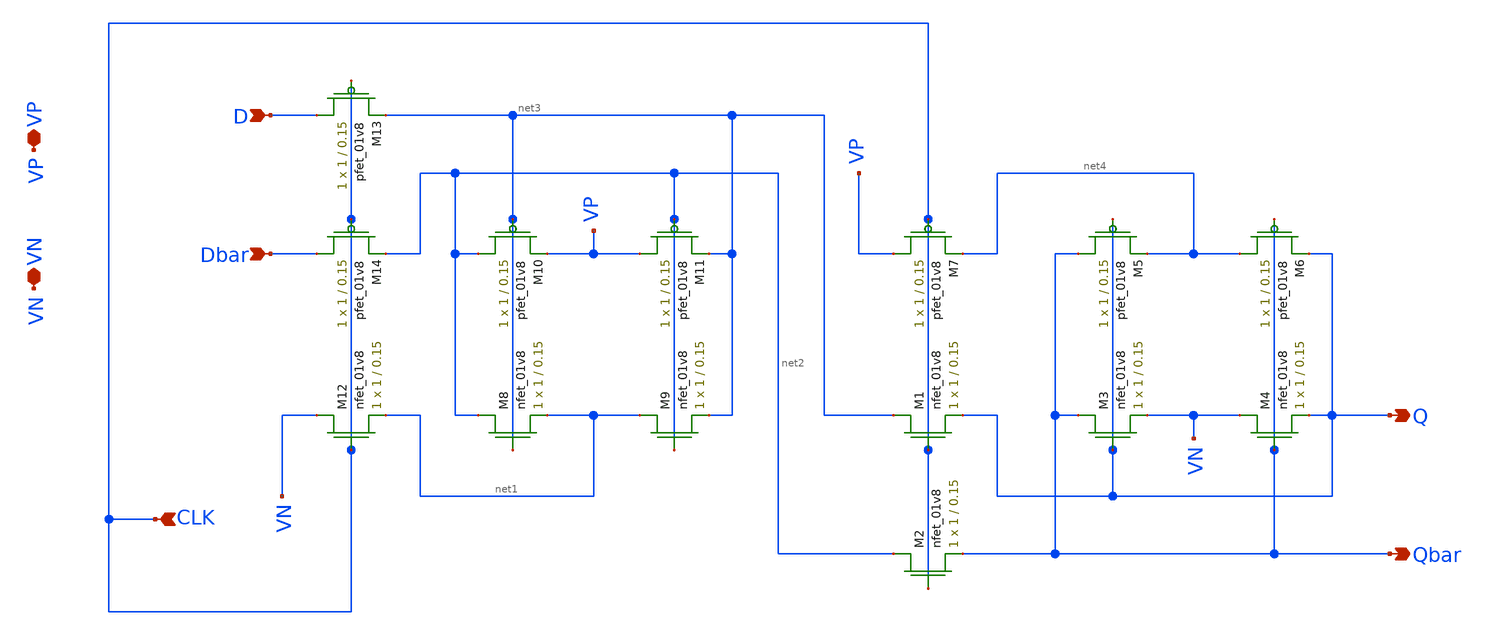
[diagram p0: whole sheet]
** sch_path: mp2/xschem/flipflop/flipflop_layout.sch
**.subckt flipflop_layout D Dbar Q Qbar CLK VP VN
*.ipin D
*.ipin Dbar
*.opin Q
*.opin Qbar
*.ipin CLK
*.iopin VP
*.iopin VN
XM1 net3 CLK Q GND sky130_fd_pr__nfet_01v8 L=0.15 W=1 nf=1 ad='int((nf+1)/2) * W/nf * 0.29' as='int((nf+2)/2) * W/nf * 0.29'
+ pd='2*int((nf+1)/2) * (W/nf + 0.29)' ps='2*int((nf+2)/2) * (W/nf + 0.29)' nrd='0.29 / W' nrs='0.29 / W'
+ sa=0 sb=0 sd=0 mult=1 m=1
XM2 net2 CLK Qbar GND sky130_fd_pr__nfet_01v8 L=0.15 W=1 nf=1 ad='int((nf+1)/2) * W/nf * 0.29' as='int((nf+2)/2) * W/nf * 0.29'
+ pd='2*int((nf+1)/2) * (W/nf + 0.29)' ps='2*int((nf+2)/2) * (W/nf + 0.29)' nrd='0.29 / W' nrs='0.29 / W'
+ sa=0 sb=0 sd=0 mult=1 m=1
XM3 Qbar Q VN GND sky130_fd_pr__nfet_01v8 L=0.15 W=1 nf=1 ad='int((nf+1)/2) * W/nf * 0.29' as='int((nf+2)/2) * W/nf * 0.29'
+ pd='2*int((nf+1)/2) * (W/nf + 0.29)' ps='2*int((nf+2)/2) * (W/nf + 0.29)' nrd='0.29 / W' nrs='0.29 / W'
+ sa=0 sb=0 sd=0 mult=1 m=1
XM4 VN Qbar Q GND sky130_fd_pr__nfet_01v8 L=0.15 W=1 nf=1 ad='int((nf+1)/2) * W/nf * 0.29' as='int((nf+2)/2) * W/nf * 0.29'
+ pd='2*int((nf+1)/2) * (W/nf + 0.29)' ps='2*int((nf+2)/2) * (W/nf + 0.29)' nrd='0.29 / W' nrs='0.29 / W'
+ sa=0 sb=0 sd=0 mult=1 m=1
XM5 Qbar Q net4 VDD sky130_fd_pr__pfet_01v8 L=0.15 W=1 nf=1 ad='int((nf+1)/2) * W/nf * 0.29' as='int((nf+2)/2) * W/nf * 0.29'
+ pd='2*int((nf+1)/2) * (W/nf + 0.29)' ps='2*int((nf+2)/2) * (W/nf + 0.29)' nrd='0.29 / W' nrs='0.29 / W'
+ sa=0 sb=0 sd=0 mult=1 m=1
XM6 net4 Qbar Q VDD sky130_fd_pr__pfet_01v8 L=0.15 W=1 nf=1 ad='int((nf+1)/2) * W/nf * 0.29' as='int((nf+2)/2) * W/nf * 0.29'
+ pd='2*int((nf+1)/2) * (W/nf + 0.29)' ps='2*int((nf+2)/2) * (W/nf + 0.29)' nrd='0.29 / W' nrs='0.29 / W'
+ sa=0 sb=0 sd=0 mult=1 m=1
XM7 VP CLK net4 VDD sky130_fd_pr__pfet_01v8 L=0.15 W=1 nf=1 ad='int((nf+1)/2) * W/nf * 0.29' as='int((nf+2)/2) * W/nf * 0.29'
+ pd='2*int((nf+1)/2) * (W/nf + 0.29)' ps='2*int((nf+2)/2) * (W/nf + 0.29)' nrd='0.29 / W' nrs='0.29 / W'
+ sa=0 sb=0 sd=0 mult=1 m=1
XM8 net2 net3 net1 GND sky130_fd_pr__nfet_01v8 L=0.15 W=1 nf=1 ad='int((nf+1)/2) * W/nf * 0.29' as='int((nf+2)/2) * W/nf * 0.29'
+ pd='2*int((nf+1)/2) * (W/nf + 0.29)' ps='2*int((nf+2)/2) * (W/nf + 0.29)' nrd='0.29 / W' nrs='0.29 / W'
+ sa=0 sb=0 sd=0 mult=1 m=1
XM9 net1 net2 net3 GND sky130_fd_pr__nfet_01v8 L=0.15 W=1 nf=1 ad='int((nf+1)/2) * W/nf * 0.29' as='int((nf+2)/2) * W/nf * 0.29'
+ pd='2*int((nf+1)/2) * (W/nf + 0.29)' ps='2*int((nf+2)/2) * (W/nf + 0.29)' nrd='0.29 / W' nrs='0.29 / W'
+ sa=0 sb=0 sd=0 mult=1 m=1
XM10 net2 net3 VP VDD sky130_fd_pr__pfet_01v8 L=0.15 W=1 nf=1 ad='int((nf+1)/2) * W/nf * 0.29' as='int((nf+2)/2) * W/nf * 0.29'
+ pd='2*int((nf+1)/2) * (W/nf + 0.29)' ps='2*int((nf+2)/2) * (W/nf + 0.29)' nrd='0.29 / W' nrs='0.29 / W'
+ sa=0 sb=0 sd=0 mult=1 m=1
XM11 VP net2 net3 VDD sky130_fd_pr__pfet_01v8 L=0.15 W=1 nf=1 ad='int((nf+1)/2) * W/nf * 0.29' as='int((nf+2)/2) * W/nf * 0.29'
+ pd='2*int((nf+1)/2) * (W/nf + 0.29)' ps='2*int((nf+2)/2) * (W/nf + 0.29)' nrd='0.29 / W' nrs='0.29 / W'
+ sa=0 sb=0 sd=0 mult=1 m=1
XM12 VN CLK net1 GND sky130_fd_pr__nfet_01v8 L=0.15 W=1 nf=1 ad='int((nf+1)/2) * W/nf * 0.29' as='int((nf+2)/2) * W/nf * 0.29'
+ pd='2*int((nf+1)/2) * (W/nf + 0.29)' ps='2*int((nf+2)/2) * (W/nf + 0.29)' nrd='0.29 / W' nrs='0.29 / W'
+ sa=0 sb=0 sd=0 mult=1 m=1
XM13 D CLK net3 VDD sky130_fd_pr__pfet_01v8 L=0.15 W=1 nf=1 ad='int((nf+1)/2) * W/nf * 0.29' as='int((nf+2)/2) * W/nf * 0.29'
+ pd='2*int((nf+1)/2) * (W/nf + 0.29)' ps='2*int((nf+2)/2) * (W/nf + 0.29)' nrd='0.29 / W' nrs='0.29 / W'
+ sa=0 sb=0 sd=0 mult=1 m=1
XM14 Dbar CLK net2 VDD sky130_fd_pr__pfet_01v8 L=0.15 W=1 nf=1 ad='int((nf+1)/2) * W/nf * 0.29' as='int((nf+2)/2) * W/nf * 0.29'
+ pd='2*int((nf+1)/2) * (W/nf + 0.29)' ps='2*int((nf+2)/2) * (W/nf + 0.29)' nrd='0.29 / W' nrs='0.29 / W'
+ sa=0 sb=0 sd=0 mult=1 m=1
**.ends
.end
